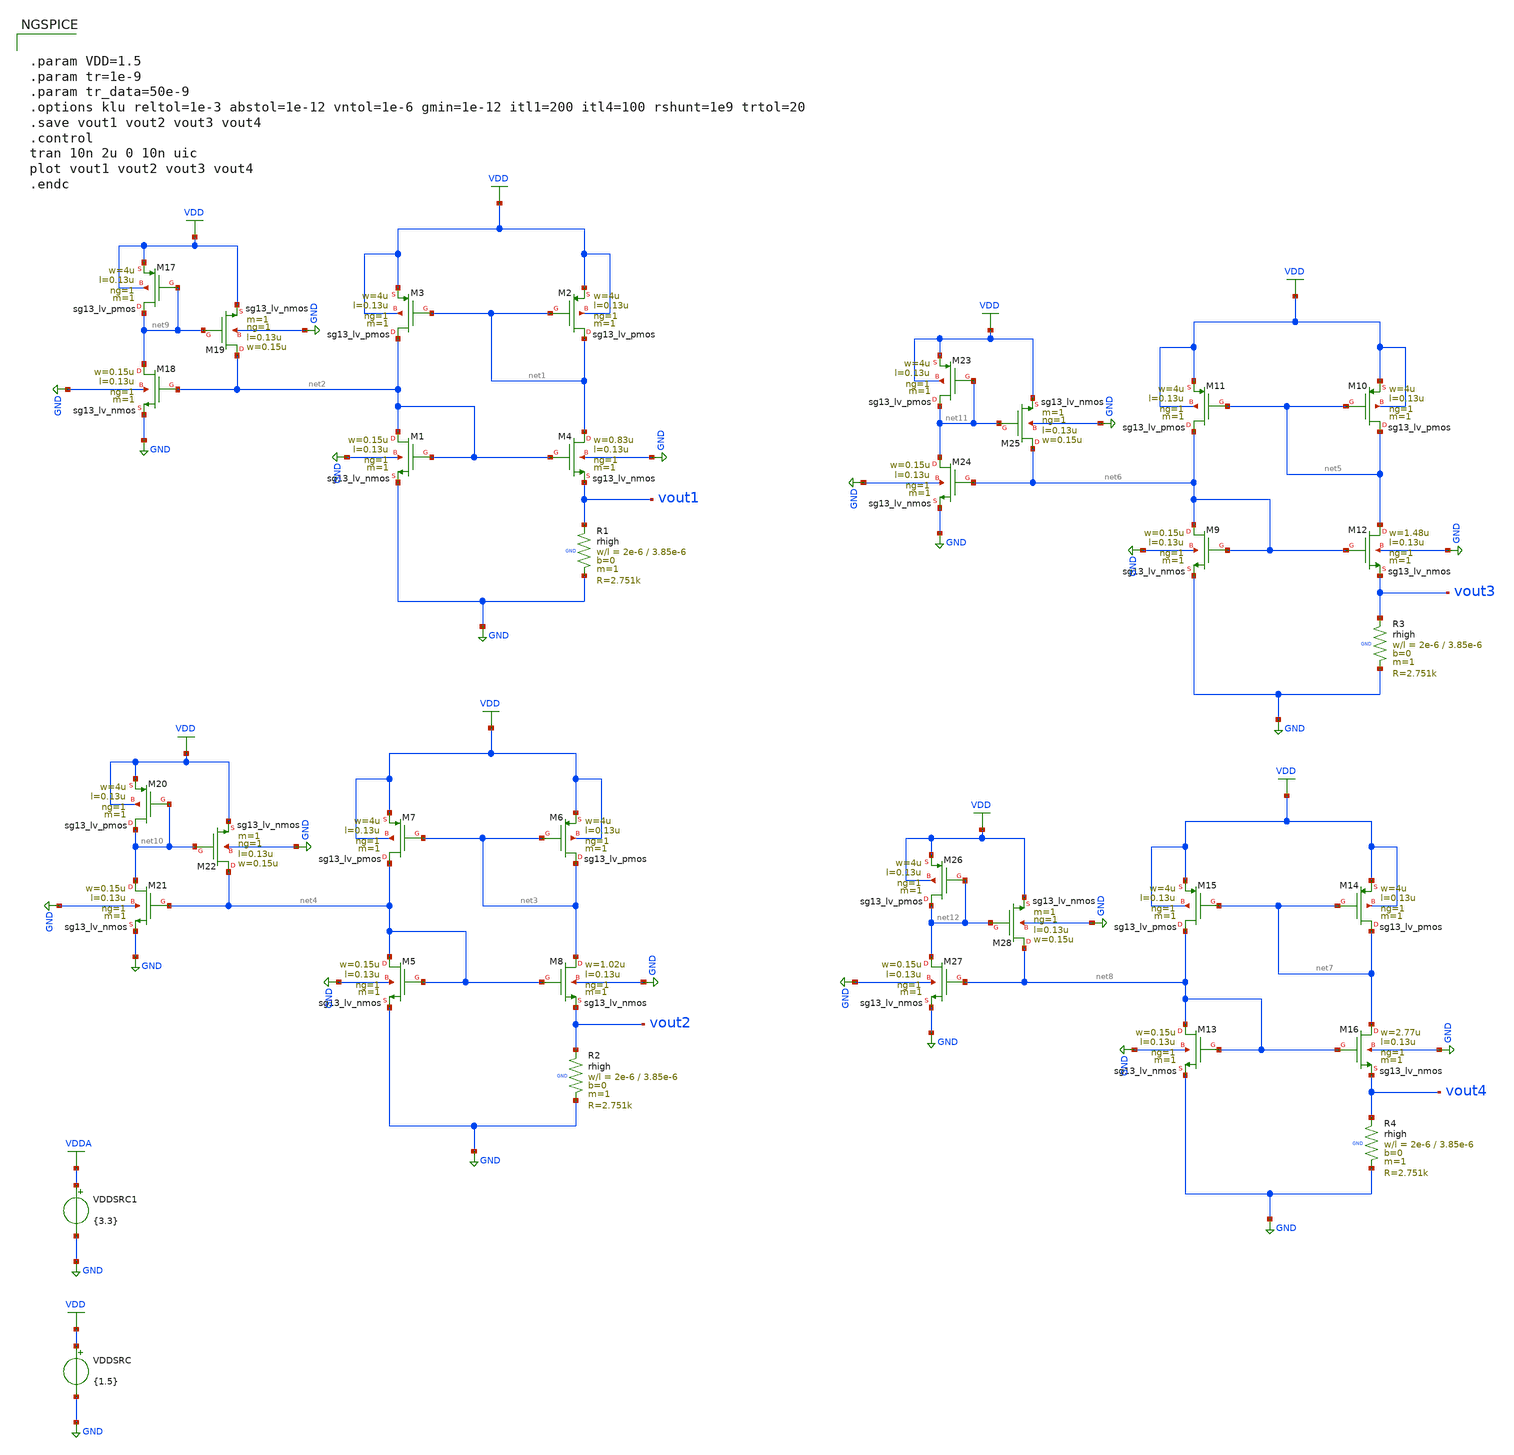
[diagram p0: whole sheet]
** sch_path: macros/heichips26_ook_top/testbenches/xschem/b_mult_tb_tran.sch
**.subckt b_mult_tb_tran
VDDSRC VDD GND {1.5}
VDDSRC1 VDDA GND {3.3}
XM1 net2 net2 GND GND sg13_lv_nmos w=0.15u l=0.13u ng=1 m=1 mm_ok=1
XM2 net1 net1 VDD VDD sg13_lv_pmos w=4u l=0.13u ng=1 m=1 mm_ok=1
XR1 vout1 GND GND rhigh w=2e-6 l=3.85e-6 m=1 b=0 mm_ok=1
XM3 net2 net1 VDD VDD sg13_lv_pmos w=4u l=0.13u ng=1 m=1 mm_ok=1
XM4 net1 net2 vout1 GND sg13_lv_nmos w=0.83u l=0.13u ng=1 m=1 mm_ok=1
XM5 net4 net4 GND GND sg13_lv_nmos w=0.15u l=0.13u ng=1 m=1 mm_ok=1
XM6 net3 net3 VDD VDD sg13_lv_pmos w=4u l=0.13u ng=1 m=1 mm_ok=1
XR2 vout2 GND GND rhigh w=2e-6 l=3.85e-6 m=1 b=0 mm_ok=1
XM7 net4 net3 VDD VDD sg13_lv_pmos w=4u l=0.13u ng=1 m=1 mm_ok=1
XM8 net3 net4 vout2 GND sg13_lv_nmos w=1.02u l=0.13u ng=1 m=1 mm_ok=1
XM9 net6 net6 GND GND sg13_lv_nmos w=0.15u l=0.13u ng=1 m=1 mm_ok=1
XM10 net5 net5 VDD VDD sg13_lv_pmos w=4u l=0.13u ng=1 m=1 mm_ok=1
XR3 vout3 GND GND rhigh w=2e-6 l=3.85e-6 m=1 b=0 mm_ok=1
XM11 net6 net5 VDD VDD sg13_lv_pmos w=4u l=0.13u ng=1 m=1 mm_ok=1
XM12 net5 net6 vout3 GND sg13_lv_nmos w=1.48u l=0.13u ng=1 m=1 mm_ok=1
XM13 net8 net8 GND GND sg13_lv_nmos w=0.15u l=0.13u ng=1 m=1 mm_ok=1
XM14 net7 net7 VDD VDD sg13_lv_pmos w=4u l=0.13u ng=1 m=1 mm_ok=1
XR4 vout4 GND GND rhigh w=2e-6 l=3.85e-6 m=1 b=0 mm_ok=1
XM15 net8 net7 VDD VDD sg13_lv_pmos w=4u l=0.13u ng=1 m=1 mm_ok=1
XM16 net7 net8 vout4 GND sg13_lv_nmos w=2.77u l=0.13u ng=1 m=1 mm_ok=1
XM17 net9 net9 VDD VDD sg13_lv_pmos w=4u l=0.13u ng=1 m=1 mm_ok=1
XM18 net9 net2 GND GND sg13_lv_nmos w=0.15u l=0.13u ng=1 m=1 mm_ok=1
XM19 net2 net9 VDD GND sg13_lv_nmos w=0.15u l=0.13u ng=1 m=1 mm_ok=1
XM20 net10 net10 VDD VDD sg13_lv_pmos w=4u l=0.13u ng=1 m=1 mm_ok=1
XM21 net10 net4 GND GND sg13_lv_nmos w=0.15u l=0.13u ng=1 m=1 mm_ok=1
XM22 net4 net10 VDD GND sg13_lv_nmos w=0.15u l=0.13u ng=1 m=1 mm_ok=1
XM23 net11 net11 VDD VDD sg13_lv_pmos w=4u l=0.13u ng=1 m=1 mm_ok=1
XM24 net11 net6 GND GND sg13_lv_nmos w=0.15u l=0.13u ng=1 m=1 mm_ok=1
XM25 net6 net11 VDD GND sg13_lv_nmos w=0.15u l=0.13u ng=1 m=1 mm_ok=1
XM26 net12 net12 VDD VDD sg13_lv_pmos w=4u l=0.13u ng=1 m=1 mm_ok=1
XM27 net12 net8 GND GND sg13_lv_nmos w=0.15u l=0.13u ng=1 m=1 mm_ok=1
XM28 net8 net12 VDD GND sg13_lv_nmos w=0.15u l=0.13u ng=1 m=1 mm_ok=1
**** begin user architecture code


.param VDD=1.5
.param tr=1e-9
.param tr_data=50e-9
.options klu reltol=1e-3 abstol=1e-12 vntol=1e-6 gmin=1e-12 itl1=200 itl4=100 rshunt=1e9 trtol=20
.save vout1 vout2 vout3 vout4
.control
tran 10n 2u 0 10n uic
plot vout1 vout2 vout3 vout4
.endc



.lib cornerMOSlv.lib mos_tt
.lib cornerMOShv.lib mos_tt
.lib cornerRES.lib res_typ
.lib cornerDIO.lib dio_tt
.lib cornerCAP.lib cap_typ
.include /home/belal/HeiChips/heichips26-on-off/macros/heichips26_ook_top/macros/dac/netlist/xspice/dac.xspice
.include /home/belal/HeiChips/heichips26-on-off/macros/heichips26_ook_top/macros/ook_analog_system/netlist/pex/ook_transmitter_magic_pex_3.spice
.include /home/belal/HeiChips/heichips26-on-off/macros/heichips26_ook_top/macros/ook_analog_system/netlist/pex/ook_analog_system_magic_pex_3.spice
.include /home/belal/HeiChips/heichips26-on-off/IHP-Open-PDK/ihp-sg13cmos5l/libs.tech/ngspice/models/cap_mfringe.lib
.include /home/belal/HeiChips/heichips26-on-off/macros/heichips26_ook_top/macros/ook_analog_system/netlist/pex/vco_magic_pex_3.spice
.include /home/belal/HeiChips/heichips26-on-off/macros/heichips26_ook_top/macros/ook_analog_system/netlist/pex/output_buffer_magic_pex_3.spice
.include /home/belal/HeiChips/heichips26-on-off/macros/heichips26_ook_top/netlist/pex/heichips26_ook_top_magic_pex_3.spice
.include /home/belal/HeiChips/heichips26-on-off/IHP-Open-PDK/ihp-sg13cmos5l/libs.ref/sg13cmos5l_io/spice/sg13cmos5l_io.spi

**** end user architecture code
**.ends
.GLOBAL VDD
.GLOBAL GND
.GLOBAL VDDA
.end
